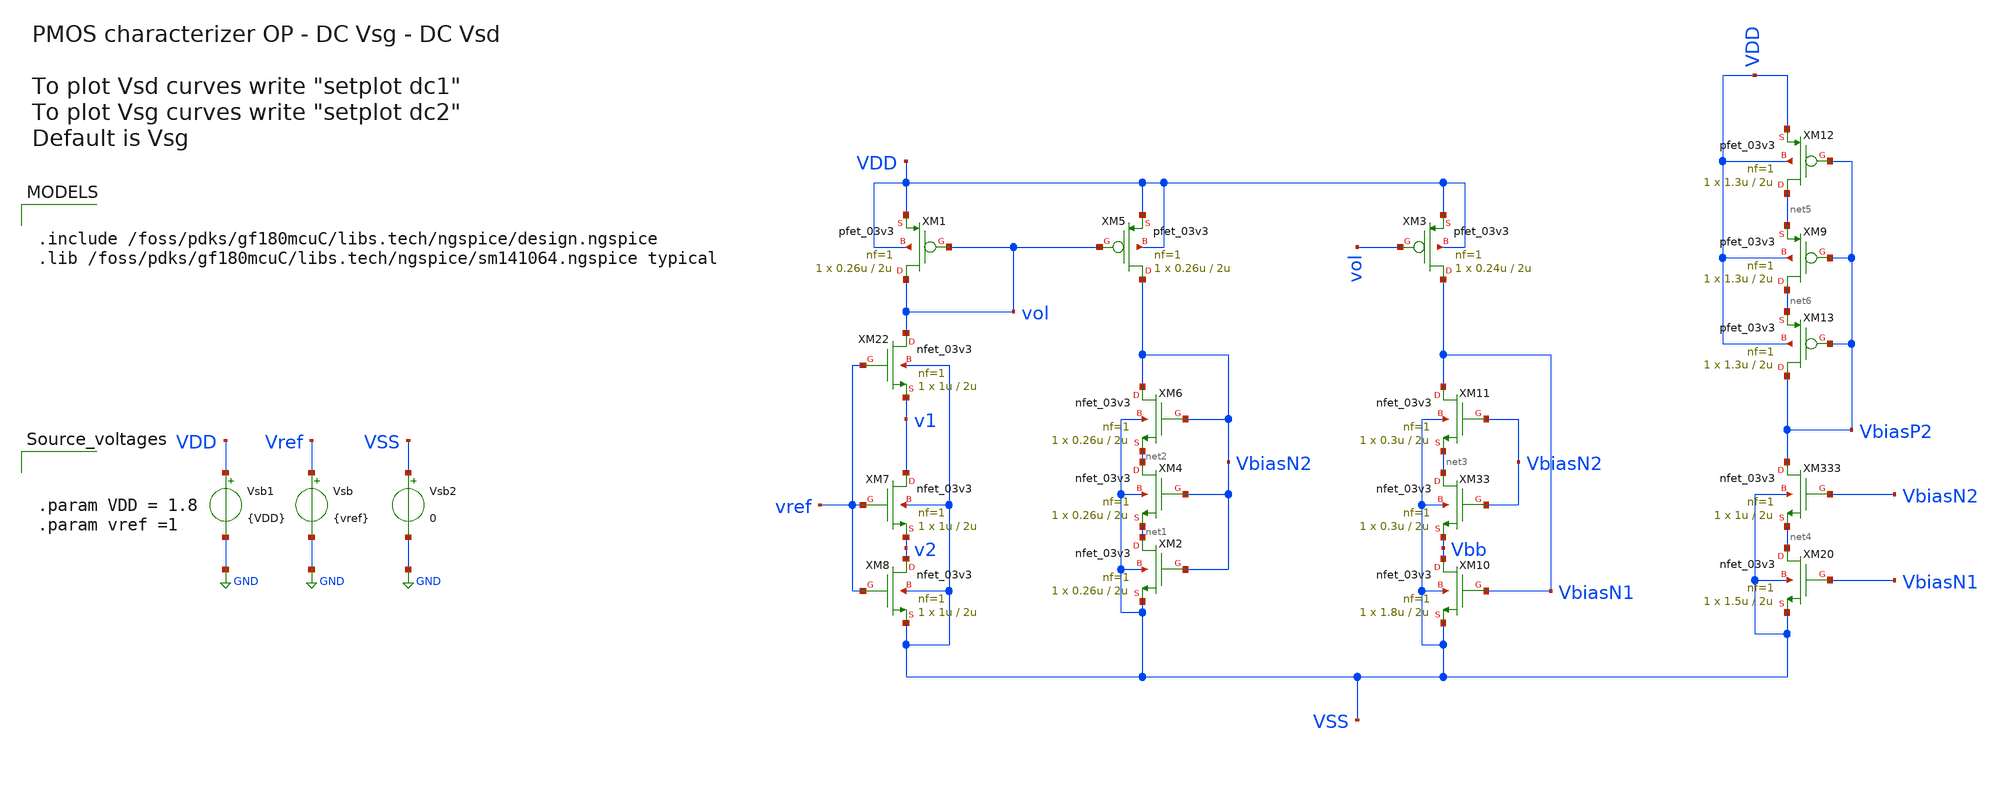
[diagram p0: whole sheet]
** sch_path: designs/used_and_to_delete/error_amplifier_bias_bradly/xschem/primeraprueba_bias.sch
**.subckt primeraprueba_bias
XM1 vol vol VDD VDD pfet_03v3 L=2u W=0.26u nf=1 ad='int((nf+1)/2) * W/nf * 0.18u' as='int((nf+2)/2) * W/nf * 0.18u'
+ pd='2*int((nf+1)/2) * (W/nf + 0.18u)' ps='2*int((nf+2)/2) * (W/nf + 0.18u)' nrd='0.18u / W' nrs='0.18u / W'
+ sa=0 sb=0 sd=0 m=1
Vsb1 VDD GND {VDD}
XM22 vol vref v1 VSS nfet_03v3 L=2u W=1u nf=1 ad='int((nf+1)/2) * W/nf * 0.18u' as='int((nf+2)/2) * W/nf * 0.18u'
+ pd='2*int((nf+1)/2) * (W/nf + 0.18u)' ps='2*int((nf+2)/2) * (W/nf + 0.18u)' nrd='0.18u / W' nrs='0.18u / W'
+ sa=0 sb=0 sd=0 m=1
Vsb Vref GND {vref}
XM5 VbiasN2 vol VDD VDD pfet_03v3 L=2u W=0.26u nf=1 ad='int((nf+1)/2) * W/nf * 0.18u' as='int((nf+2)/2) * W/nf * 0.18u'
+ pd='2*int((nf+1)/2) * (W/nf + 0.18u)' ps='2*int((nf+2)/2) * (W/nf + 0.18u)' nrd='0.18u / W' nrs='0.18u / W'
+ sa=0 sb=0 sd=0 m=1
XM2 net1 VbiasN2 VSS VSS nfet_03v3 L=2u W=0.26u nf=1 ad='int((nf+1)/2) * W/nf * 0.18u' as='int((nf+2)/2) * W/nf * 0.18u'
+ pd='2*int((nf+1)/2) * (W/nf + 0.18u)' ps='2*int((nf+2)/2) * (W/nf + 0.18u)' nrd='0.18u / W' nrs='0.18u / W'
+ sa=0 sb=0 sd=0 m=1
XM7 v1 vref v2 VSS nfet_03v3 L=2u W=1u nf=1 ad='int((nf+1)/2) * W/nf * 0.18u' as='int((nf+2)/2) * W/nf * 0.18u'
+ pd='2*int((nf+1)/2) * (W/nf + 0.18u)' ps='2*int((nf+2)/2) * (W/nf + 0.18u)' nrd='0.18u / W' nrs='0.18u / W'
+ sa=0 sb=0 sd=0 m=1
XM8 v2 vref VSS VSS nfet_03v3 L=2u W=1u nf=1 ad='int((nf+1)/2) * W/nf * 0.18u' as='int((nf+2)/2) * W/nf * 0.18u'
+ pd='2*int((nf+1)/2) * (W/nf + 0.18u)' ps='2*int((nf+2)/2) * (W/nf + 0.18u)' nrd='0.18u / W' nrs='0.18u / W'
+ sa=0 sb=0 sd=0 m=1
XM4 net2 VbiasN2 net1 VSS nfet_03v3 L=2u W=0.26u nf=1 ad='int((nf+1)/2) * W/nf * 0.18u' as='int((nf+2)/2) * W/nf * 0.18u'
+ pd='2*int((nf+1)/2) * (W/nf + 0.18u)' ps='2*int((nf+2)/2) * (W/nf + 0.18u)' nrd='0.18u / W' nrs='0.18u / W'
+ sa=0 sb=0 sd=0 m=1
XM6 VbiasN2 VbiasN2 net2 VSS nfet_03v3 L=2u W=0.26u nf=1 ad='int((nf+1)/2) * W/nf * 0.18u' as='int((nf+2)/2) * W/nf * 0.18u'
+ pd='2*int((nf+1)/2) * (W/nf + 0.18u)' ps='2*int((nf+2)/2) * (W/nf + 0.18u)' nrd='0.18u / W' nrs='0.18u / W'
+ sa=0 sb=0 sd=0 m=1
XM3 VbiasN1 vol VDD VDD pfet_03v3 L=2u W=0.24u nf=1 ad='int((nf+1)/2) * W/nf * 0.18u' as='int((nf+2)/2) * W/nf * 0.18u'
+ pd='2*int((nf+1)/2) * (W/nf + 0.18u)' ps='2*int((nf+2)/2) * (W/nf + 0.18u)' nrd='0.18u / W' nrs='0.18u / W'
+ sa=0 sb=0 sd=0 m=1
XM10 Vbb VbiasN1 VSS VSS nfet_03v3 L=2u W=1.8u nf=1 ad='int((nf+1)/2) * W/nf * 0.18u' as='int((nf+2)/2) * W/nf * 0.18u'
+ pd='2*int((nf+1)/2) * (W/nf + 0.18u)' ps='2*int((nf+2)/2) * (W/nf + 0.18u)' nrd='0.18u / W' nrs='0.18u / W'
+ sa=0 sb=0 sd=0 m=1
XM11 VbiasN1 VbiasN2 net3 VSS nfet_03v3 L=2u W=0.3u nf=1 ad='int((nf+1)/2) * W/nf * 0.18u' as='int((nf+2)/2) * W/nf * 0.18u'
+ pd='2*int((nf+1)/2) * (W/nf + 0.18u)' ps='2*int((nf+2)/2) * (W/nf + 0.18u)' nrd='0.18u / W' nrs='0.18u / W'
+ sa=0 sb=0 sd=0 m=1
XM33 net3 VbiasN2 Vbb VSS nfet_03v3 L=2u W=0.3u nf=1 ad='int((nf+1)/2) * W/nf * 0.18u' as='int((nf+2)/2) * W/nf * 0.18u'
+ pd='2*int((nf+1)/2) * (W/nf + 0.18u)' ps='2*int((nf+2)/2) * (W/nf + 0.18u)' nrd='0.18u / W' nrs='0.18u / W'
+ sa=0 sb=0 sd=0 m=1
XM333 VbiasP2 VbiasN2 net4 VSS nfet_03v3 L=2u W=1u nf=1 ad='int((nf+1)/2) * W/nf * 0.18u' as='int((nf+2)/2) * W/nf * 0.18u'
+ pd='2*int((nf+1)/2) * (W/nf + 0.18u)' ps='2*int((nf+2)/2) * (W/nf + 0.18u)' nrd='0.18u / W' nrs='0.18u / W'
+ sa=0 sb=0 sd=0 m=1
XM20 net4 VbiasN1 VSS VSS nfet_03v3 L=2u W=1.5u nf=1 ad='int((nf+1)/2) * W/nf * 0.18u' as='int((nf+2)/2) * W/nf * 0.18u'
+ pd='2*int((nf+1)/2) * (W/nf + 0.18u)' ps='2*int((nf+2)/2) * (W/nf + 0.18u)' nrd='0.18u / W' nrs='0.18u / W'
+ sa=0 sb=0 sd=0 m=1
XM12 net5 VbiasP2 VDD VDD pfet_03v3 L=2u W=1.3u nf=1 ad='int((nf+1)/2) * W/nf * 0.18u' as='int((nf+2)/2) * W/nf * 0.18u'
+ pd='2*int((nf+1)/2) * (W/nf + 0.18u)' ps='2*int((nf+2)/2) * (W/nf + 0.18u)' nrd='0.18u / W' nrs='0.18u / W'
+ sa=0 sb=0 sd=0 m=1
XM9 net6 VbiasP2 net5 VDD pfet_03v3 L=2u W=1.3u nf=1 ad='int((nf+1)/2) * W/nf * 0.18u' as='int((nf+2)/2) * W/nf * 0.18u'
+ pd='2*int((nf+1)/2) * (W/nf + 0.18u)' ps='2*int((nf+2)/2) * (W/nf + 0.18u)' nrd='0.18u / W' nrs='0.18u / W'
+ sa=0 sb=0 sd=0 m=1
XM13 VbiasP2 VbiasP2 net6 VDD pfet_03v3 L=2u W=1.3u nf=1 ad='int((nf+1)/2) * W/nf * 0.18u' as='int((nf+2)/2) * W/nf * 0.18u'
+ pd='2*int((nf+1)/2) * (W/nf + 0.18u)' ps='2*int((nf+2)/2) * (W/nf + 0.18u)' nrd='0.18u / W' nrs='0.18u / W'
+ sa=0 sb=0 sd=0 m=1
Vsb2 VSS GND 0
**** begin user architecture code

.include /foss/pdks/gf180mcuC/libs.tech/ngspice/design.ngspice
.lib /foss/pdks/gf180mcuC/libs.tech/ngspice/sm141064.ngspice typical




.param VDD = 1.8
.param vref =1






*save data for dc simulation
.save @m.xm1.m0[id]
.save @m.xm1.m0[gm]
.save @m.xm1.m0[gds]
.save @m.xm1.m0[cgg]
.save @m.xm1.m0[cdd]
.save @m.xm1.m0[vgs]
.save @m.xm1.m0[vds]
.save @m.xm1.m0[vbs]
.save @m.xm1.m0[vth]
.save @m.xm1.m0[vdsat]

.save @m.xm3.m0[id]
.save @m.xm3.m0[gm]
.save @m.xm3.m0[gds]
.save @m.xm3.m0[cgg]
.save @m.xm3.m0[cdd]
.save @m.xm3.m0[vgs]
.save @m.xm3.m0[vds]
.save @m.xm3.m0[vbs]
.save @m.xm3.m0[vth]
.save @m.xm3.m0[vdsat]

.save @m.xm2.m0[id]
.save @m.xm2.m0[gm]
.save @m.xm2.m0[gds]
.save @m.xm2.m0[cgg]
.save @m.xm2.m0[cdd]
.save @m.xm2.m0[vgs]
.save @m.xm2.m0[vds]
.save @m.xm2.m0[vbs]
.save @m.xm2.m0[vth]
.save @m.xm2.m0[vdsat]

.save @m.xm4.m0[id]
.save @m.xm4.m0[gm]
.save @m.xm4.m0[gds]
.save @m.xm4.m0[cgg]
.save @m.xm4.m0[cdd]
.save @m.xm4.m0[vgs]
.save @m.xm4.m0[vds]
.save @m.xm4.m0[vbs]
.save @m.xm4.m0[vth]
.save @m.xm4.m0[vdsat]

.save @m.xm5.m0[id]
.save @m.xm5.m0[gm]
.save @m.xm5.m0[gds]
.save @m.xm5.m0[cgg]
.save @m.xm5.m0[cdd]
.save @m.xm5.m0[vgs]
.save @m.xm5.m0[vds]
.save @m.xm5.m0[vbs]
.save @m.xm5.m0[vth]
.save @m.xm5.m0[vdsat]

.control
save all

** Simulation
op
dc Vsd 0 1.8 0.01
dc Vsg 0 1.8 0.01

** Print op
setplot op1

let id = @m.xm1.m0[id]
let gm = @m.xm1.m0[gm]
let ro = 1/@m.xm1.m0[gds]
let Vsg = -@m.xm1.m0[vgs]
let Vsd = -@m.xm1.m0[vds]
let Vbs = -@m.xm1.m0[vbs]
let Vdsat = @m.xm1.m0[vdsat]
let Vth = @m.xm1.m0[vth]
let Vov = Vsg - abs(Vth)
let varVsd = Vsd - abs(Vdsat)
let ao = gm*ro
let gmid = gm/id
let Cgg = @m.xm1.m0[cgg]
let Cdd = @m.xm1.m0[cdd]
let fT = gm/(6.283185*Cgg)

let id_3 = @m.xm3.m0[id]
let gm_3 = @m.xm3.m0[gm]
let ro_3 = 1/@m.xm3.m0[gds]
let Vgs_3 = @m.xm3.m0[vgs]
let Vds_3 = @m.xm3.m0[vds]
let Vbs_3 = @m.xm3.m0[vbs]
let Vdsat_3 = @m.xm3.m0[vdsat]
let Vth_3 = @m.xm3.m0[vth]
let Vov_3 = Vsg_3 - abs(Vth_3)
let varVsd_3 = Vsd_3 - abs(Vdsat_3)
let ao_3 = gm_3 * ro_3
let gmid_3 = gm_3 / id_3
let Cgg_3 = @m.xm3.m0[cgg]
let Cdd_3 = @m.xm3.m0[cdd]
let fT_3 = gm_3 / (6.283185 * Cgg_3)

let id_2 = @m.xm2.m0[id]
let gm_2 = @m.xm2.m0[gm]
let ro_2 = 1/@m.xm2.m0[gds]
let Vgs_2 = @m.xm2.m0[vgs]
let Vds_2 = @m.xm2.m0[vds]
let Vbs_2 = -@m.xm2.m0[vbs]
let Vdsat_2 = @m.xm2.m0[vdsat]
let Vth_2 = @m.xm2.m0[vth]
let Vov_2 = Vsg_2 - abs(Vth_2)
let varVsd_2 = Vsd_2 - abs(Vdsat_2)
let ao_2 = gm_2 * ro_2
let gmid_2 = gm_2 / id_2
let Cgg_2 = @m.xm2.m0[cgg]
let Cdd_2 = @m.xm2.m0[cdd]
let fT_2 = gm_2 / (6.283185 * Cgg_2)

let id_4 = @m.xm4.m0[id]
let gm_4 = @m.xm4.m0[gm]
let ro_4 = 1/@m.xm4.m0[gds]
let Vgs_4 = @m.xm4.m0[vgs]
let Vds_4 = @m.xm4.m0[vds]
let Vbs_4 = -@m.xm4.m0[vbs]
let Vdsat_4 = @m.xm4.m0[vdsat]
let Vth_4 = @m.xm4.m0[vth]
let Vov_4 = Vsg_4 - abs(Vth_4)
let varVsd_4 = Vsd_4 - abs(Vdsat_4)
let ao_4 = gm_4 * ro_4
let gmid_4 = gm_4 / id_4
let Cgg_4 = @m.xm4.m0[cgg]
let Cdd_4 = @m.xm4.m0[cdd]
let fT_4 = gm_4 / (6.283185 * Cgg_4)

let id_5 = @m.xm5.m0[id]
let gm_5 = @m.xm5.m0[gm]
let ro_5 = 1/@m.xm5.m0[gds]
let Vgs_5 = @m.xm5.m0[vgs]
let Vds_5 = @m.xm5.m0[vds]
let Vbs_5 = -@m.xm5.m0[vbs]
let Vdsat_5 = @m.xm5.m0[vdsat]
let Vth_5 = @m.xm5.m0[vth]
let Vov_5 = Vsg_5 - abs(Vth_5)
let varVsd_5 = Vsd_5 - abs(Vdsat_5)
let ao_5 = gm_5 * ro_5
let gmid_5 = gm_5 / id_5
let Cgg_5 = @m.xm5.m0[cgg]
let Cdd_5 = @m.xm5.m0[cdd]
let fT_5 = gm_5 / (6.283185 * Cgg_5)

let region_1 = Vsg - Vth
let region_2 = Vgs_2 - Vth_2
let region_3 = Vgs_3 - Vth_3
let region_4 = Vgs_4 -Vth_4
let region_5 = Vgs_5 -Vth_5


echo
echo
echo
echo ** Datos del transistor M1
echo
print id Vsd Vsg Vth region_1 Vdsat
echo
echo
echo
echo ** Datos del transistor M2
echo
print id_2   Vds_2 Vgs_2 Vth_2  region_2

echo
echo
echo
echo ** Datos del transistor M3
echo
print id_3 Vds_3 Vgs_3 Vth_3 region_3

echo ** voltajes
print volt v1 v2 v3

write primeraprueba_bias.raw

** Plots dc Vsd
setplot dc1

let id = @m.xm1.m0[id]
let gm = @m.xm1.m0[gm]
let ro = 1/@m.xm1.m0[gds]

** Plot here the Vsd curves
*plot id

** Plots dc Vsg
setplot dc2

let id = @m.xm1.m0[id]
let gm = @m.xm1.m0[gm]
let gmid = gm/id
let ro = 1/@m.xm1.m0[gds]
let fT = gm/(6.283185*@m.xm1.m0[cgg])
let ftgmid = fT*gmid
let GfT = fT*gm*ro

** Plot here the Vsg curves

*plot id

.endc



**** end user architecture code
**.ends
.GLOBAL GND
.end
